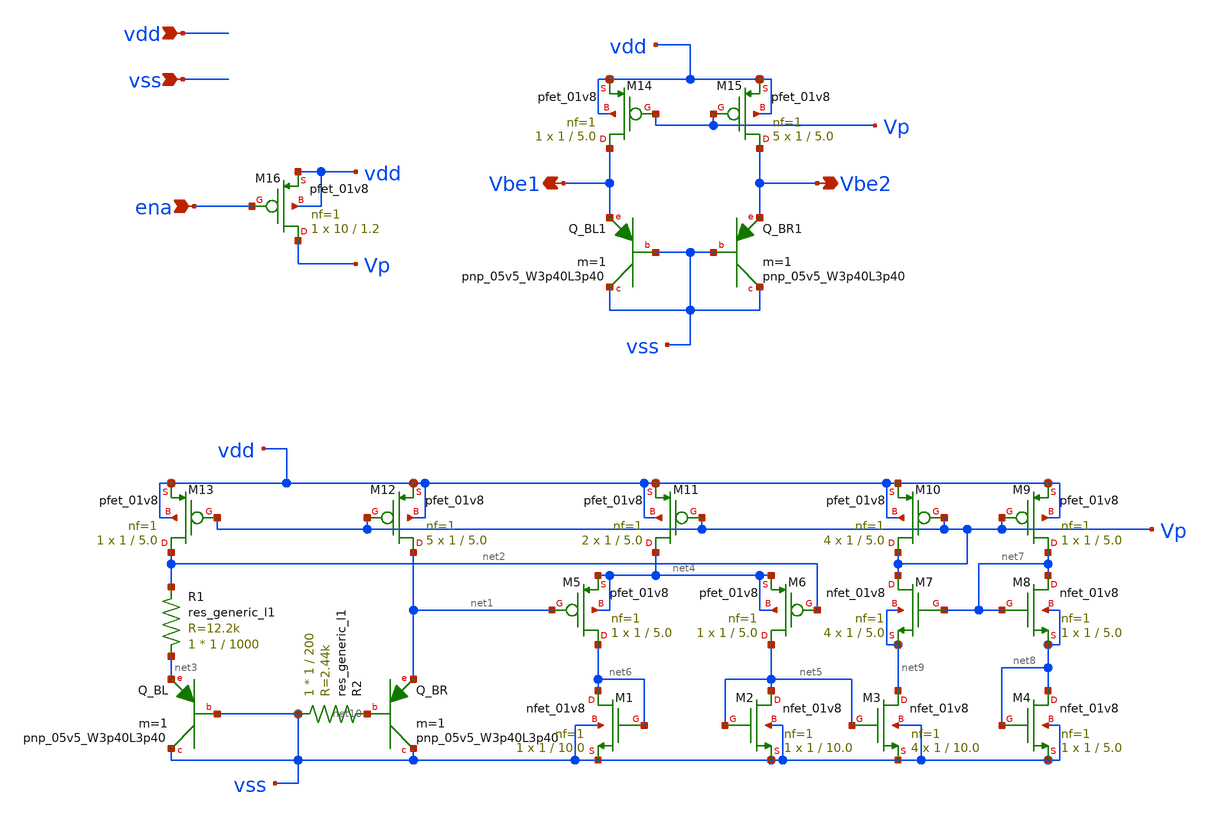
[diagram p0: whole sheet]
** sch_path: xschem/sky130_od_ip__tempsensor.sch
**.subckt sky130_od_ip__tempsensor vdd vss Vbe2 Vbe1 ena
*.ipin vdd
*.ipin vss
*.opin Vbe2
*.opin Vbe1
*.ipin ena
XM12 net1 Vp vdd vdd sky130_fd_pr__pfet_01v8 L=5.0 W=1 nf=1 ad='int((nf+1)/2) * W/nf * 0.29' as='int((nf+2)/2) * W/nf * 0.29'
+ pd='2*int((nf+1)/2) * (W/nf + 0.29)' ps='2*int((nf+2)/2) * (W/nf + 0.29)' nrd='0.29 / W' nrs='0.29 / W'
+ sa=0 sb=0 sd=0 mult=5 m=5
XM13 net2 Vp vdd vdd sky130_fd_pr__pfet_01v8 L=5.0 W=1 nf=1 ad='int((nf+1)/2) * W/nf * 0.29' as='int((nf+2)/2) * W/nf * 0.29'
+ pd='2*int((nf+1)/2) * (W/nf + 0.29)' ps='2*int((nf+2)/2) * (W/nf + 0.29)' nrd='0.29 / W' nrs='0.29 / W'
+ sa=0 sb=0 sd=0 mult=1 m=1
XQ_BR vss net10 net1 sky130_fd_pr__pnp_05v5_W3p40L3p40 m=1
XQ_BL vss vss net3 sky130_fd_pr__pnp_05v5_W3p40L3p40 m=1
XM11 net4 Vp vdd vdd sky130_fd_pr__pfet_01v8 L=5.0 W=1 nf=1 ad='int((nf+1)/2) * W/nf * 0.29' as='int((nf+2)/2) * W/nf * 0.29'
+ pd='2*int((nf+1)/2) * (W/nf + 0.29)' ps='2*int((nf+2)/2) * (W/nf + 0.29)' nrd='0.29 / W' nrs='0.29 / W'
+ sa=0 sb=0 sd=0 mult=2 m=2
XM6 net5 net2 net4 net4 sky130_fd_pr__pfet_01v8 L=5.0 W=1 nf=1 ad='int((nf+1)/2) * W/nf * 0.29' as='int((nf+2)/2) * W/nf * 0.29'
+ pd='2*int((nf+1)/2) * (W/nf + 0.29)' ps='2*int((nf+2)/2) * (W/nf + 0.29)' nrd='0.29 / W' nrs='0.29 / W'
+ sa=0 sb=0 sd=0 mult=1 m=1
XM5 net6 net1 net4 net4 sky130_fd_pr__pfet_01v8 L=5.0 W=1 nf=1 ad='int((nf+1)/2) * W/nf * 0.29' as='int((nf+2)/2) * W/nf * 0.29'
+ pd='2*int((nf+1)/2) * (W/nf + 0.29)' ps='2*int((nf+2)/2) * (W/nf + 0.29)' nrd='0.29 / W' nrs='0.29 / W'
+ sa=0 sb=0 sd=0 mult=1 m=1
XM2 net5 net5 vss vss sky130_fd_pr__nfet_01v8 L=10.0 W=1 nf=1 ad='int((nf+1)/2) * W/nf * 0.29' as='int((nf+2)/2) * W/nf * 0.29'
+ pd='2*int((nf+1)/2) * (W/nf + 0.29)' ps='2*int((nf+2)/2) * (W/nf + 0.29)' nrd='0.29 / W' nrs='0.29 / W'
+ sa=0 sb=0 sd=0 mult=1 m=1
XM1 net6 net6 vss vss sky130_fd_pr__nfet_01v8 L=10.0 W=1 nf=1 ad='int((nf+1)/2) * W/nf * 0.29' as='int((nf+2)/2) * W/nf * 0.29'
+ pd='2*int((nf+1)/2) * (W/nf + 0.29)' ps='2*int((nf+2)/2) * (W/nf + 0.29)' nrd='0.29 / W' nrs='0.29 / W'
+ sa=0 sb=0 sd=0 mult=1 m=1
XM9 net7 Vp vdd vdd sky130_fd_pr__pfet_01v8 L=5.0 W=1 nf=1 ad='int((nf+1)/2) * W/nf * 0.29' as='int((nf+2)/2) * W/nf * 0.29'
+ pd='2*int((nf+1)/2) * (W/nf + 0.29)' ps='2*int((nf+2)/2) * (W/nf + 0.29)' nrd='0.29 / W' nrs='0.29 / W'
+ sa=0 sb=0 sd=0 mult=1 m=1
XM10 Vp Vp vdd vdd sky130_fd_pr__pfet_01v8 L=5.0 W=1 nf=1 ad='int((nf+1)/2) * W/nf * 0.29' as='int((nf+2)/2) * W/nf * 0.29'
+ pd='2*int((nf+1)/2) * (W/nf + 0.29)' ps='2*int((nf+2)/2) * (W/nf + 0.29)' nrd='0.29 / W' nrs='0.29 / W'
+ sa=0 sb=0 sd=0 mult=4 m=4
XM7 Vp net7 net9 net9 sky130_fd_pr__nfet_01v8 L=5.0 W=1 nf=1 ad='int((nf+1)/2) * W/nf * 0.29' as='int((nf+2)/2) * W/nf * 0.29'
+ pd='2*int((nf+1)/2) * (W/nf + 0.29)' ps='2*int((nf+2)/2) * (W/nf + 0.29)' nrd='0.29 / W' nrs='0.29 / W'
+ sa=0 sb=0 sd=0 mult=4 m=4
XM8 net7 net7 net8 net8 sky130_fd_pr__nfet_01v8 L=5.0 W=1 nf=1 ad='int((nf+1)/2) * W/nf * 0.29' as='int((nf+2)/2) * W/nf * 0.29'
+ pd='2*int((nf+1)/2) * (W/nf + 0.29)' ps='2*int((nf+2)/2) * (W/nf + 0.29)' nrd='0.29 / W' nrs='0.29 / W'
+ sa=0 sb=0 sd=0 mult=1 m=1
XM3 net9 net5 vss vss sky130_fd_pr__nfet_01v8 L=10.0 W=1 nf=1 ad='int((nf+1)/2) * W/nf * 0.29' as='int((nf+2)/2) * W/nf * 0.29'
+ pd='2*int((nf+1)/2) * (W/nf + 0.29)' ps='2*int((nf+2)/2) * (W/nf + 0.29)' nrd='0.29 / W' nrs='0.29 / W'
+ sa=0 sb=0 sd=0 mult=4 m=4
XM4 net8 net8 vss vss sky130_fd_pr__nfet_01v8 L=5.0 W=1 nf=1 ad='int((nf+1)/2) * W/nf * 0.29' as='int((nf+2)/2) * W/nf * 0.29'
+ pd='2*int((nf+1)/2) * (W/nf + 0.29)' ps='2*int((nf+2)/2) * (W/nf + 0.29)' nrd='0.29 / W' nrs='0.29 / W'
+ sa=0 sb=0 sd=0 mult=1 m=1
XQ_BL1 vss vss Vbe1 sky130_fd_pr__pnp_05v5_W3p40L3p40 m=1
XQ_BR1 vss vss Vbe2 sky130_fd_pr__pnp_05v5_W3p40L3p40 m=1
XM14 Vbe1 Vp vdd vdd sky130_fd_pr__pfet_01v8 L=5.0 W=1 nf=1 ad='int((nf+1)/2) * W/nf * 0.29' as='int((nf+2)/2) * W/nf * 0.29'
+ pd='2*int((nf+1)/2) * (W/nf + 0.29)' ps='2*int((nf+2)/2) * (W/nf + 0.29)' nrd='0.29 / W' nrs='0.29 / W'
+ sa=0 sb=0 sd=0 mult=1 m=1
XM15 Vbe2 Vp vdd vdd sky130_fd_pr__pfet_01v8 L=5.0 W=1 nf=1 ad='int((nf+1)/2) * W/nf * 0.29' as='int((nf+2)/2) * W/nf * 0.29'
+ pd='2*int((nf+1)/2) * (W/nf + 0.29)' ps='2*int((nf+2)/2) * (W/nf + 0.29)' nrd='0.29 / W' nrs='0.29 / W'
+ sa=0 sb=0 sd=0 mult=5 m=5
XM16 Vp ena vdd vdd sky130_fd_pr__pfet_01v8 L=1.2 W=10 nf=1 ad='int((nf+1)/2) * W/nf * 0.29' as='int((nf+2)/2) * W/nf * 0.29'
+ pd='2*int((nf+1)/2) * (W/nf + 0.29)' ps='2*int((nf+2)/2) * (W/nf + 0.29)' nrd='0.29 / W' nrs='0.29 / W'
+ sa=0 sb=0 sd=0 mult=1 m=1
R1 net3 net2 sky130_fd_pr__res_generic_l1 W=1 L=1000 m=1
R2 vss net10 sky130_fd_pr__res_generic_l1 W=1 L=200 m=1
**.ends
.end
